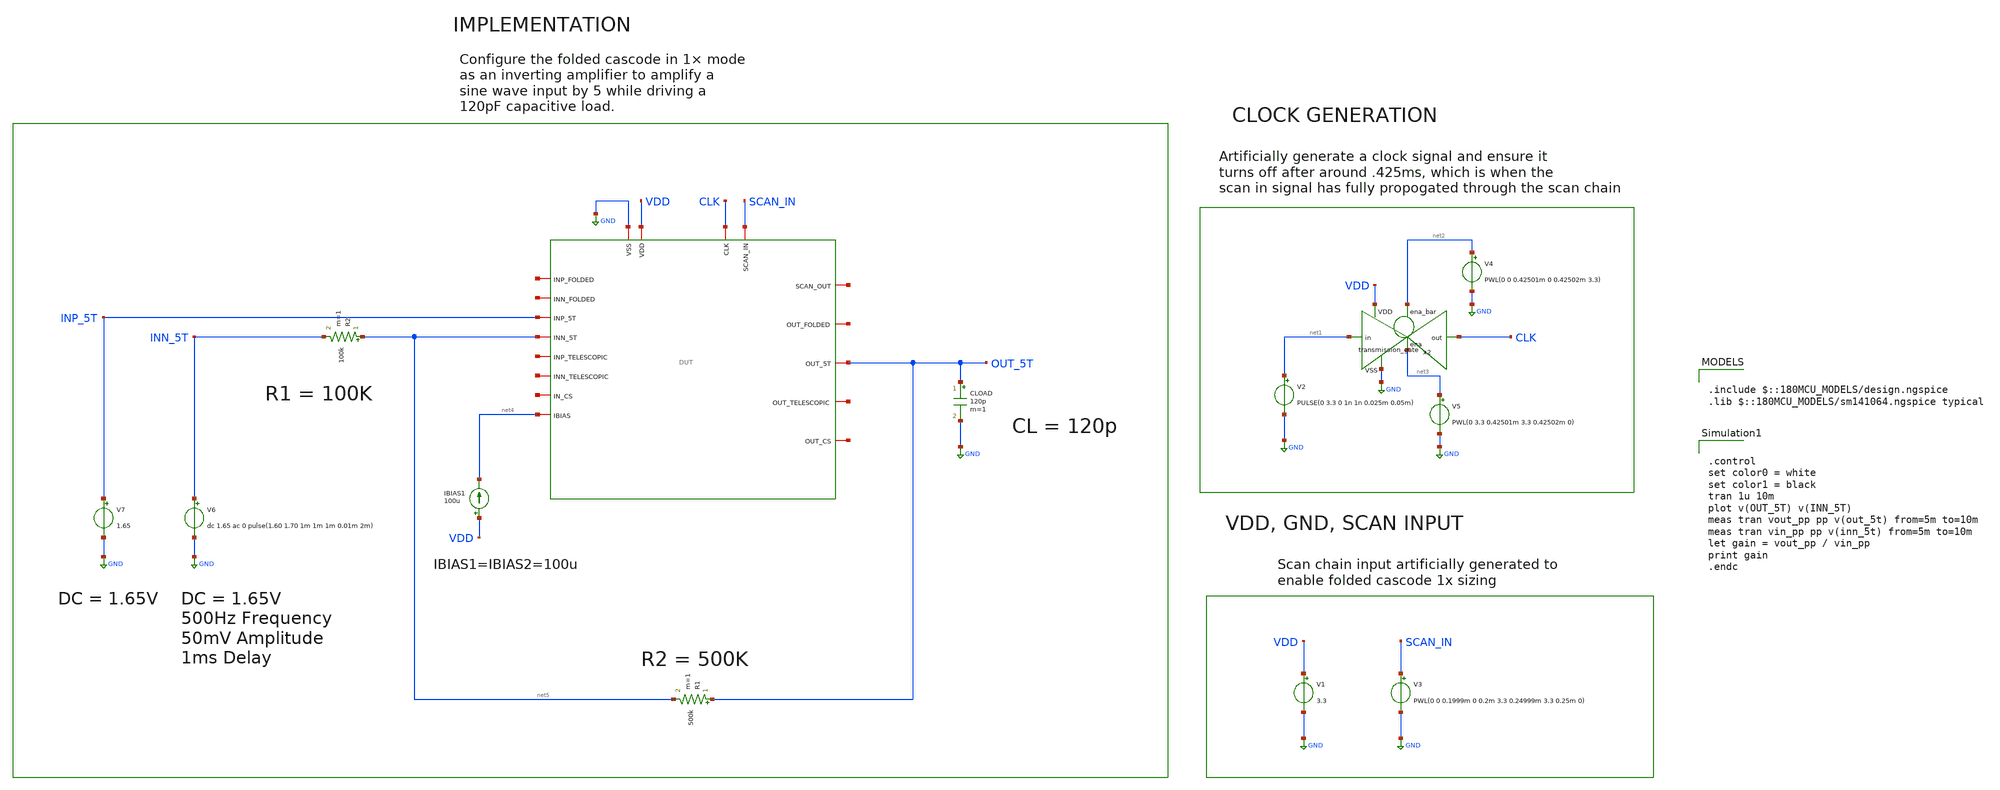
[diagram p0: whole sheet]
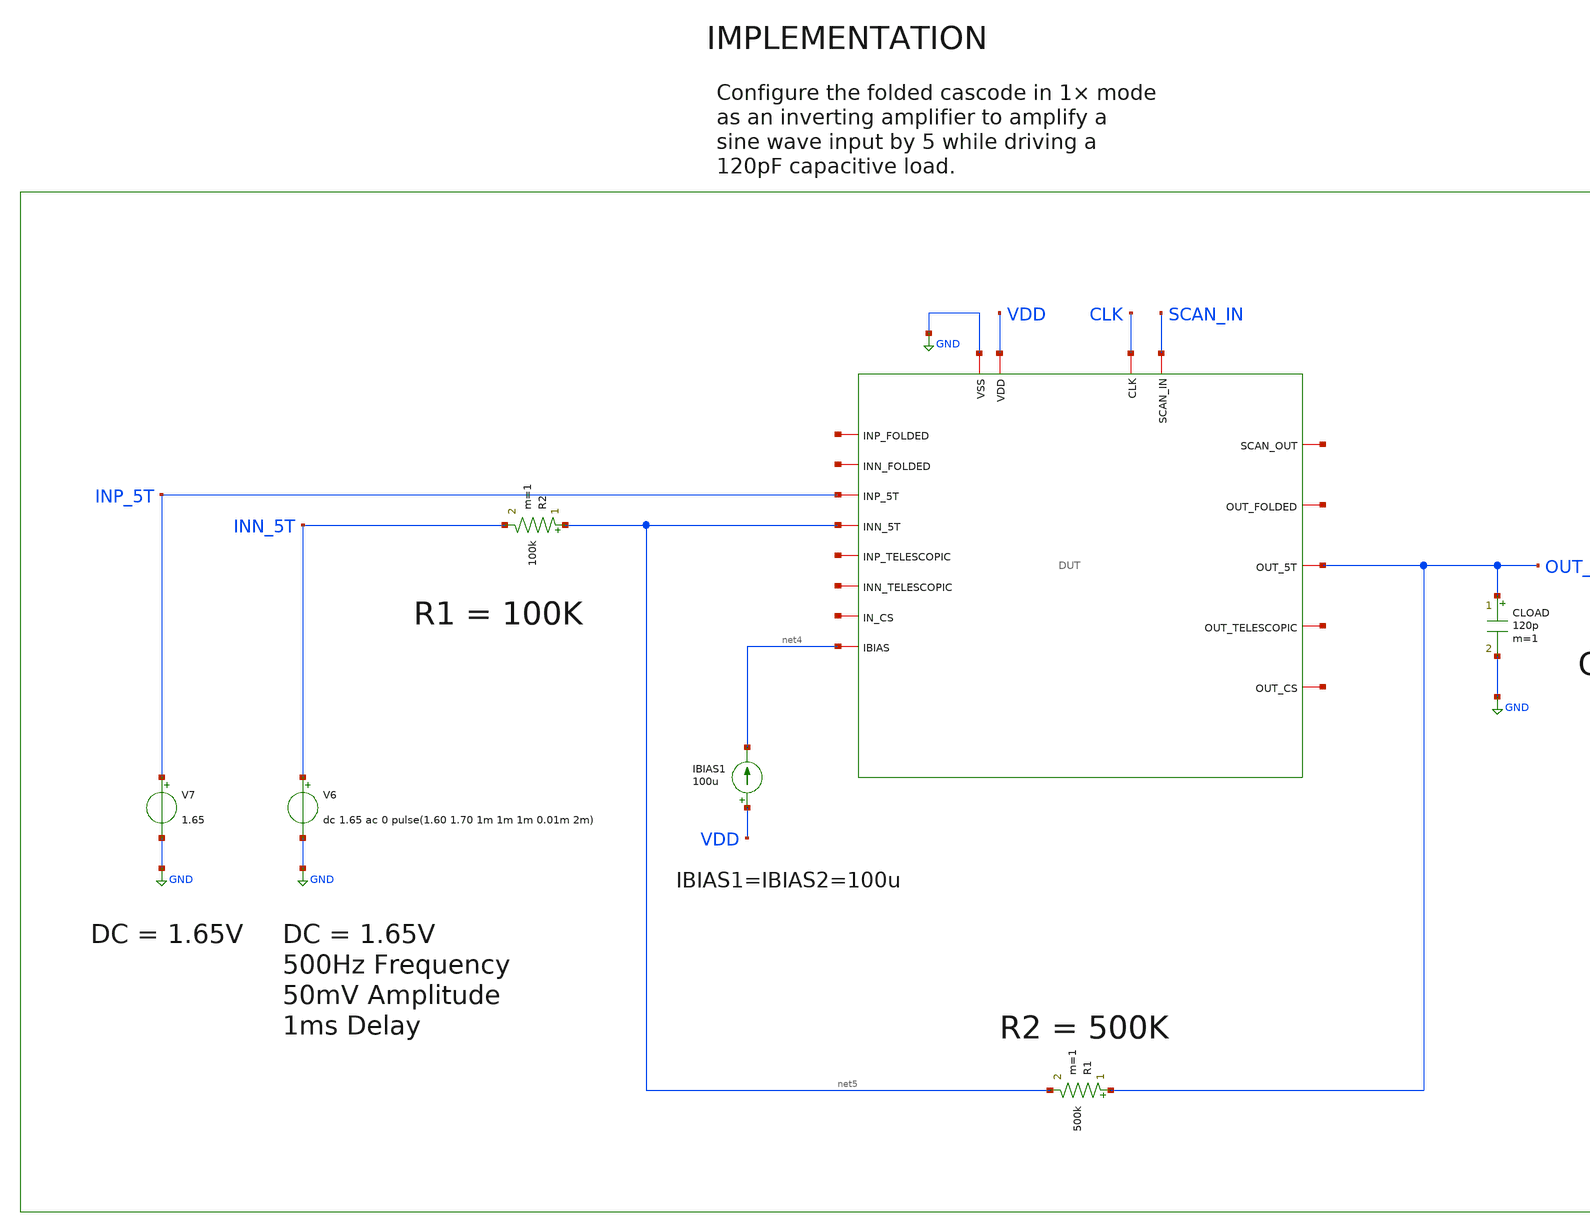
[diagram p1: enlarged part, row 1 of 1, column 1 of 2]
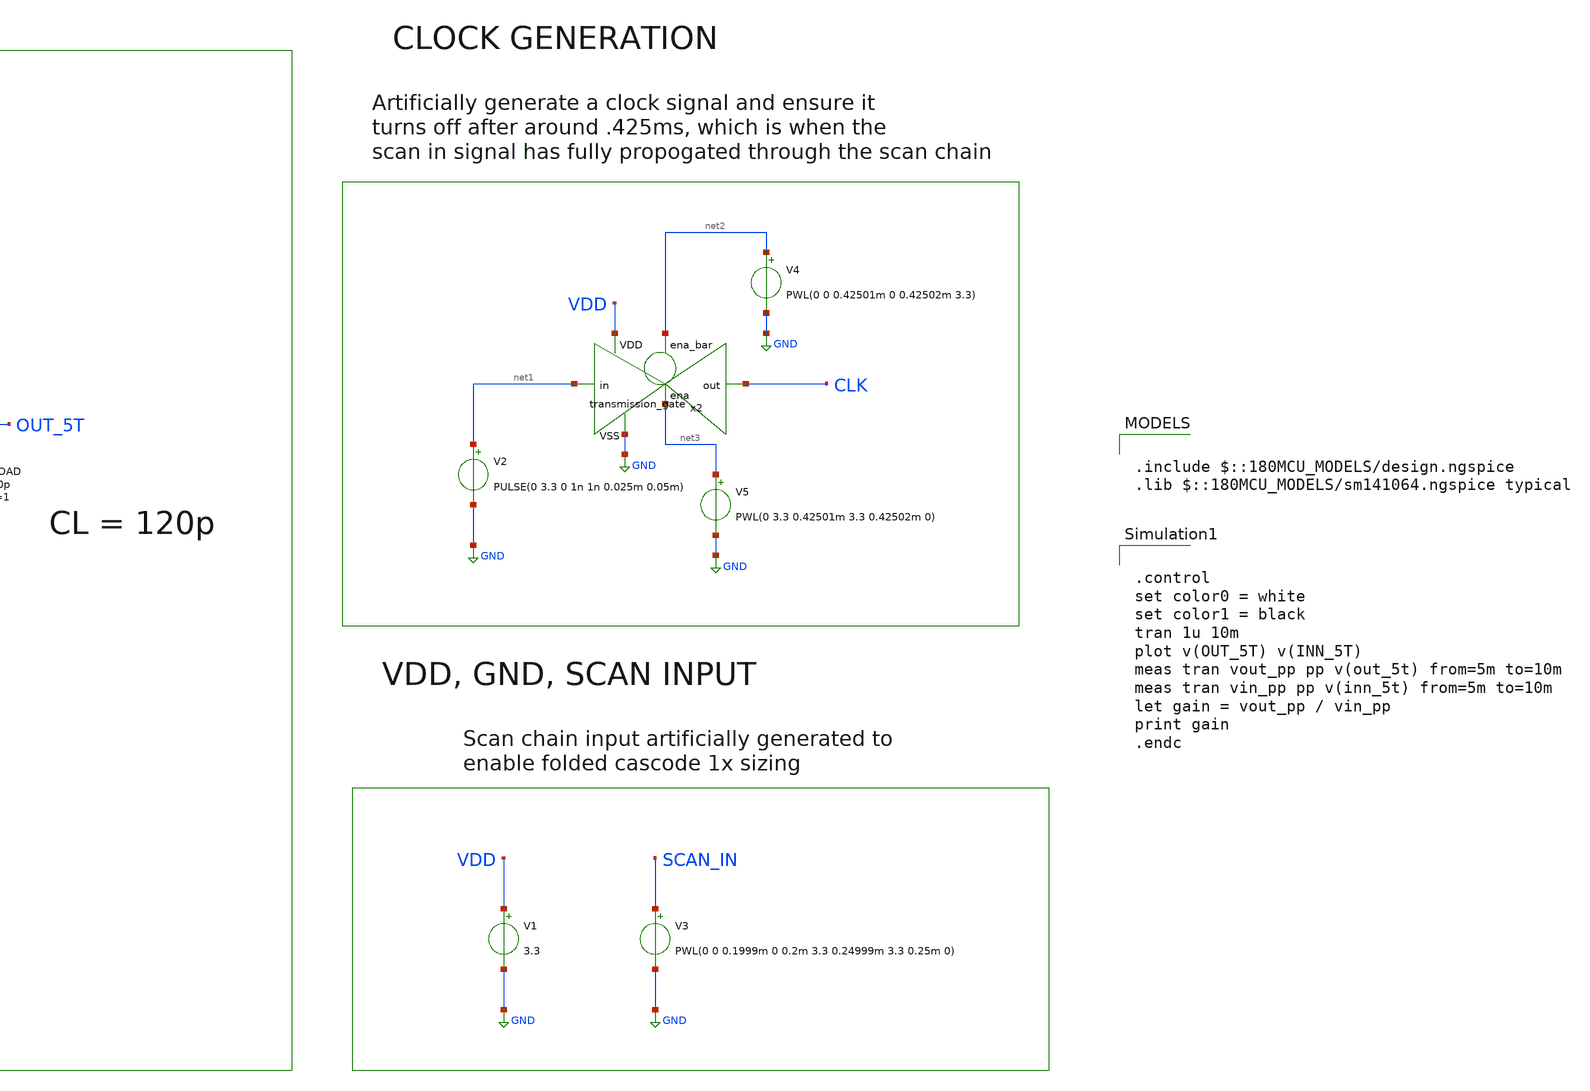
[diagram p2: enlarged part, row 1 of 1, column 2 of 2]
** sch_path: designs/libs/core_tb/sl/ota_5t/5t_inverting_triangle_1x.sch
**.subckt 5t_inverting_triangle_1x
V3 SCAN_IN GND PWL(0 0 0.1999m 0 0.2m 3.3 0.24999m 3.3 0.25m 0)
V1 VDD GND 3.3
V2 net1 GND PULSE(0 3.3 0 1n 1n 0.025m 0.05m)
x2 net2 VDD CLK net1 GND net3 transmission_gate
V4 net2 GND PWL(0 0 0.42501m 0 0.42502m 3.3)
V5 net3 GND PWL(0 3.3 0.42501m 3.3 0.42502m 0)
IBIAS1 VDD net4 100u
V7 INP_5T GND 1.65
CLOAD OUT_5T GND 120p m=1
R2 net5 INN_5T 100k m=1
V6 INN_5T GND dc 1.65 ac 0 pulse(1.60 1.70 1m 1m 1m 0.01m 2m)
R1 OUT_5T net5 500k m=1
x1 CLK net6 SCAN_IN GND VDD net7 net8 OUT_5T net4 net9 INP_5T net5 net10 net11 net12 net13 net14 DUT
**** begin user architecture code

.include $::180MCU_MODELS/design.ngspice
.lib $::180MCU_MODELS/sm141064.ngspice typical



.control
set color0 = white
set color1 = black
tran 1u 10m
plot v(OUT_5T) v(INN_5T)
meas tran vout_pp pp v(out_5t) from=5m to=10m
meas tran vin_pp pp v(inn_5t) from=5m to=10m
let gain = vout_pp / vin_pp
print gain
.endc


**** end user architecture code
**.ends
.GLOBAL GND
.end
